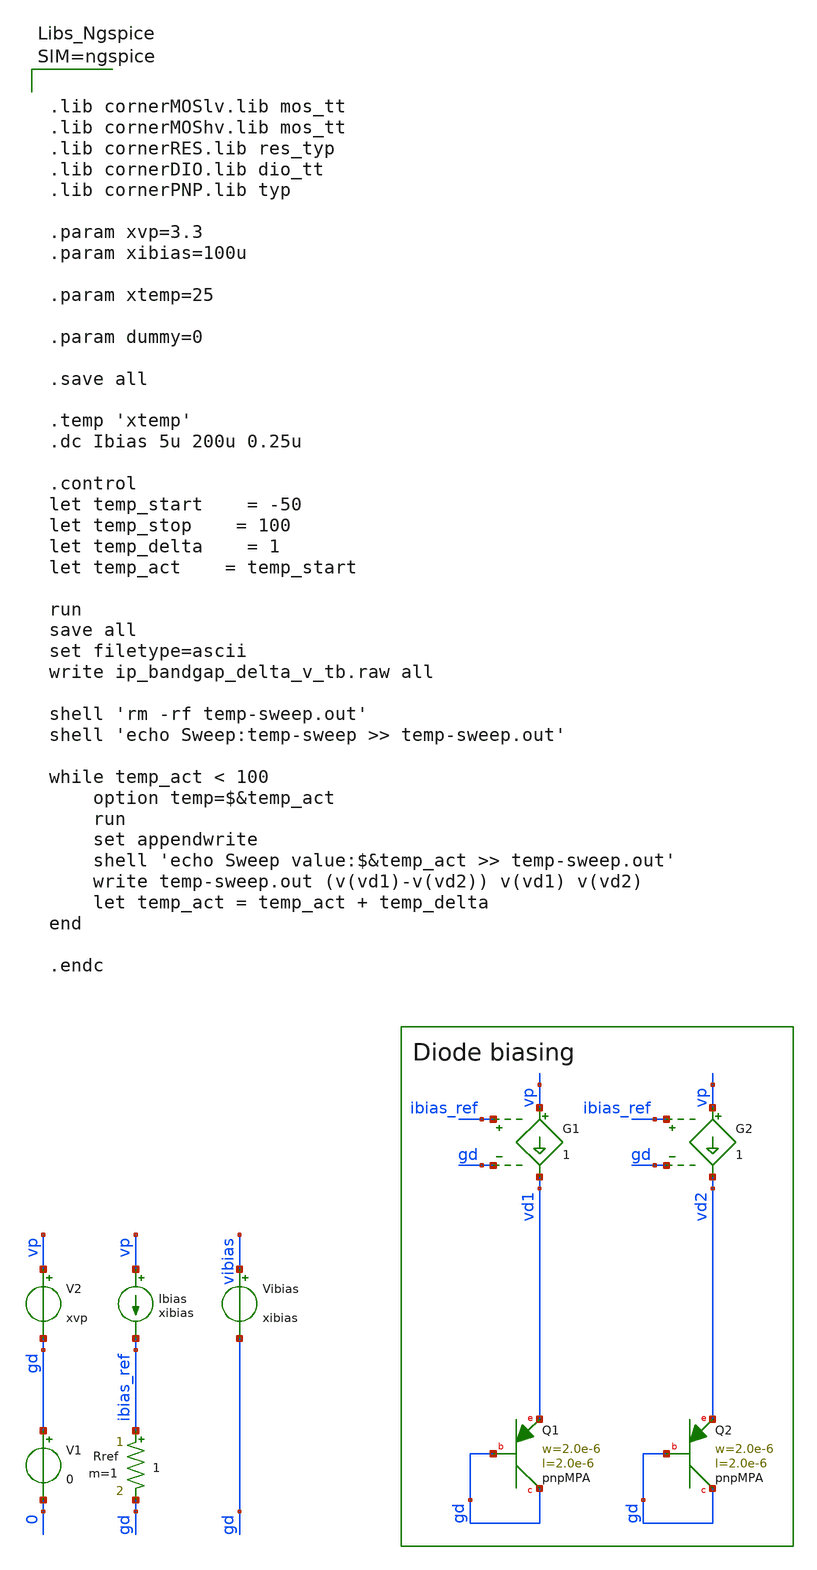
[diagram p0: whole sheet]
** sch_path: schematics/bandgap/ip_bandgap_delta_v_tb.sch
**.subckt ip_bandgap_delta_v_tb
Ibias vp ibias_ref xibias
Rref ibias_ref gd 1 m=1
V1 gd 0 0
V2 vp gd xvp
XQ1 gd gd vd1 pnpMPA a=4p p=8u m=1
XQ2 gd gd vd2 pnpMPA a=4p p=8u m=8
G1 vp vd1 ibias_ref gd 1
G2 vp vd2 ibias_ref gd 1
Vibias vibias gd xibias
**** begin user architecture code



.lib cornerMOSlv.lib mos_tt
.lib cornerMOShv.lib mos_tt
.lib cornerRES.lib res_typ
.lib cornerDIO.lib dio_tt
.lib cornerPNP.lib typ

.param xvp=3.3
.param xibias=100u

.param xtemp=25

.param dummy=0

.save all

.temp 'xtemp'
.dc Ibias 5u 200u 0.25u

.control
let temp_start	= -50
let temp_stop	= 100
let temp_delta	= 1
let temp_act	= temp_start

run
save all
set filetype=ascii
write ip_bandgap_delta_v_tb.raw all

shell 'rm -rf temp-sweep.out'
shell 'echo Sweep:temp-sweep >> temp-sweep.out'

while temp_act < 100
	option temp=$&temp_act
	run
	set appendwrite
	shell 'echo Sweep value:$&temp_act >> temp-sweep.out'
	write temp-sweep.out (v(vd1)-v(vd2)) v(vd1) v(vd2)
	let temp_act = temp_act + temp_delta
end

.endc



**** end user architecture code
**.ends
.end
